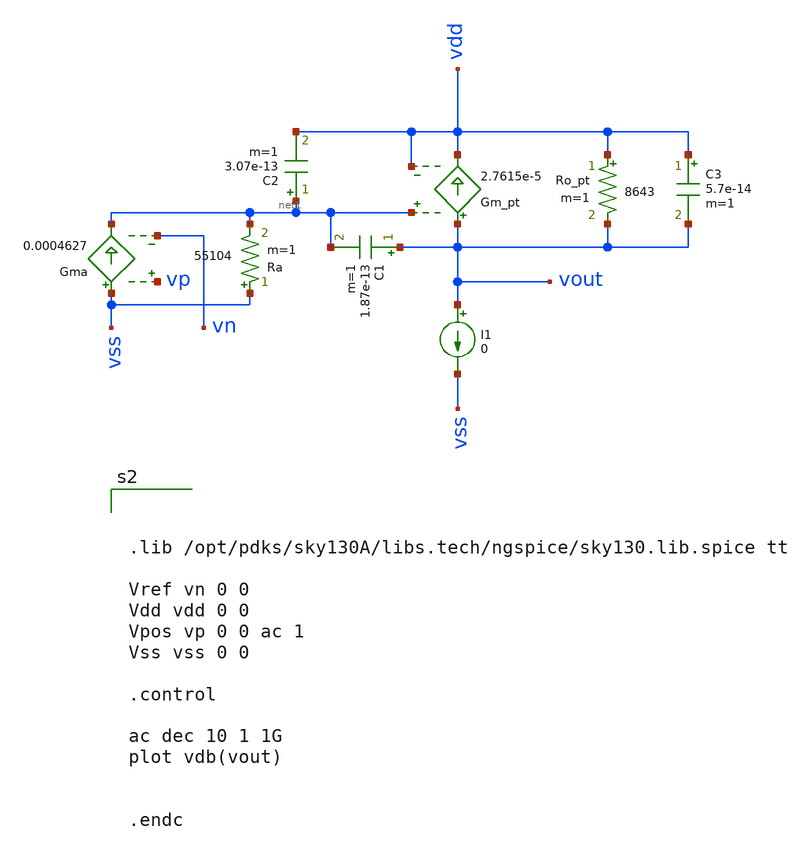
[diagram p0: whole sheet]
** sch_path: test-python/sstadex/xschem/1_cmos_ss.sch
**.subckt 1_cmos_ss
Gma vss net1 vp vn 0.0004627
Ra vss net1 55104 m=1
Ro_pt vdd vout 8643 m=1
Gm_pt vout vdd net1 vdd 2.7615e-5
C1 vout net1 1.87e-13 m=1
C2 net1 vdd 3.07e-13 m=1
I1 vout vss 0
C3 vdd vout 5.7e-14 m=1
**** begin user architecture code



.lib /opt/pdks/sky130A/libs.tech/ngspice/sky130.lib.spice tt

Vref vn 0 0
Vdd vdd 0 0
Vpos vp 0 0 ac 1
Vss vss 0 0

.control

ac dec 10 1 1G
plot vdb(vout)


.endc



**** end user architecture code
**.ends
.end
